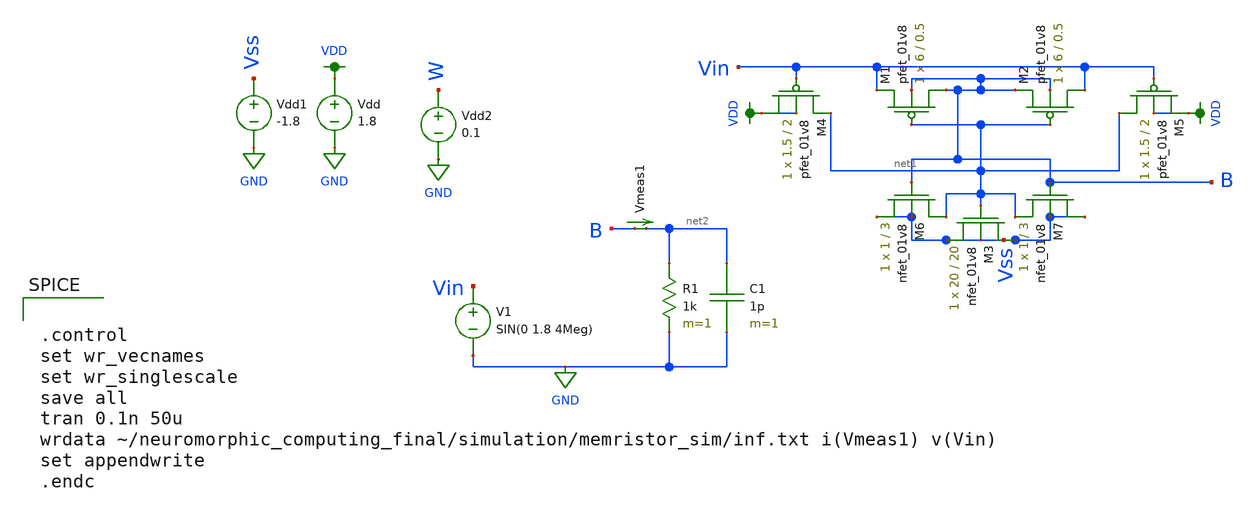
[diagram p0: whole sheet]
** sch_path: schematic/mem_lds.sch
**.subckt mem_lds
XM1 B net1 Vin B sky130_fd_pr__pfet_01v8 L=0.5 W=6 nf=1 ad='int((nf+1)/2) * W/nf * 0.29' as='int((nf+2)/2) * W/nf * 0.29'
+ pd='2*int((nf+1)/2) * (W/nf + 0.29)' ps='2*int((nf+2)/2) * (W/nf + 0.29)' nrd='0.29 / W' nrs='0.29 / W'
+ sa=0 sb=0 sd=0 mult=1 m=1
XM2 Vin net1 B B sky130_fd_pr__pfet_01v8 L=0.5 W=6 nf=1 ad='int((nf+1)/2) * W/nf * 0.29' as='int((nf+2)/2) * W/nf * 0.29'
+ pd='2*int((nf+1)/2) * (W/nf + 0.29)' ps='2*int((nf+2)/2) * (W/nf + 0.29)' nrd='0.29 / W' nrs='0.29 / W'
+ sa=0 sb=0 sd=0 mult=1 m=1
XM3 Vss net1 Vss Vss sky130_fd_pr__nfet_01v8 L=20 W=20 nf=1 ad='int((nf+1)/2) * W/nf * 0.29' as='int((nf+2)/2) * W/nf * 0.29'
+ pd='2*int((nf+1)/2) * (W/nf + 0.29)' ps='2*int((nf+2)/2) * (W/nf + 0.29)' nrd='0.29 / W' nrs='0.29 / W'
+ sa=0 sb=0 sd=0 mult=1 m=1
XM4 VDD Vin net1 VDD sky130_fd_pr__pfet_01v8 L=2 W=1.5 nf=1 ad='int((nf+1)/2) * W/nf * 0.29' as='int((nf+2)/2) * W/nf * 0.29'
+ pd='2*int((nf+1)/2) * (W/nf + 0.29)' ps='2*int((nf+2)/2) * (W/nf + 0.29)' nrd='0.29 / W' nrs='0.29 / W'
+ sa=0 sb=0 sd=0 mult=1 m=1
XM5 net1 Vin VDD VDD sky130_fd_pr__pfet_01v8 L=2 W=1.5 nf=1 ad='int((nf+1)/2) * W/nf * 0.29' as='int((nf+2)/2) * W/nf * 0.29'
+ pd='2*int((nf+1)/2) * (W/nf + 0.29)' ps='2*int((nf+2)/2) * (W/nf + 0.29)' nrd='0.29 / W' nrs='0.29 / W'
+ sa=0 sb=0 sd=0 mult=1 m=1
XM6 net1 B Vss Vss sky130_fd_pr__nfet_01v8 L=3 W=1 nf=1 ad='int((nf+1)/2) * W/nf * 0.29' as='int((nf+2)/2) * W/nf * 0.29'
+ pd='2*int((nf+1)/2) * (W/nf + 0.29)' ps='2*int((nf+2)/2) * (W/nf + 0.29)' nrd='0.29 / W' nrs='0.29 / W'
+ sa=0 sb=0 sd=0 mult=1 m=1
XM7 Vss B net1 Vss sky130_fd_pr__nfet_01v8 L=3 W=1 nf=1 ad='int((nf+1)/2) * W/nf * 0.29' as='int((nf+2)/2) * W/nf * 0.29'
+ pd='2*int((nf+1)/2) * (W/nf + 0.29)' ps='2*int((nf+2)/2) * (W/nf + 0.29)' nrd='0.29 / W' nrs='0.29 / W'
+ sa=0 sb=0 sd=0 mult=1 m=1
V1 Vin GND SIN(0 1.8 4Meg)
R1 net2 GND 1k m=1
C1 net2 GND 1p m=1
Vdd VDD GND 1.8
Vmeas1 B net2 0
.save i(vmeas1)
Vdd1 Vss GND -1.8
Vdd2 W GND 0.1
**** begin user architecture code


.control
set wr_vecnames
set wr_singlescale
save all
tran 0.1n 50u
wrdata ~/neuromorphic_computing_final/simulation/memristor_sim/inf.txt i(Vmeas1) v(Vin)
set appendwrite
.endc



.option wnflag=1
.param MC_SWITCH=0.0
.lib ~/skywater/skywater-pdk/libraries/sky130_fd_pr_ngspice/latest/models/sky130.lib.spice tt

**** end user architecture code
**.ends
.GLOBAL GND
.GLOBAL VDD
.end
